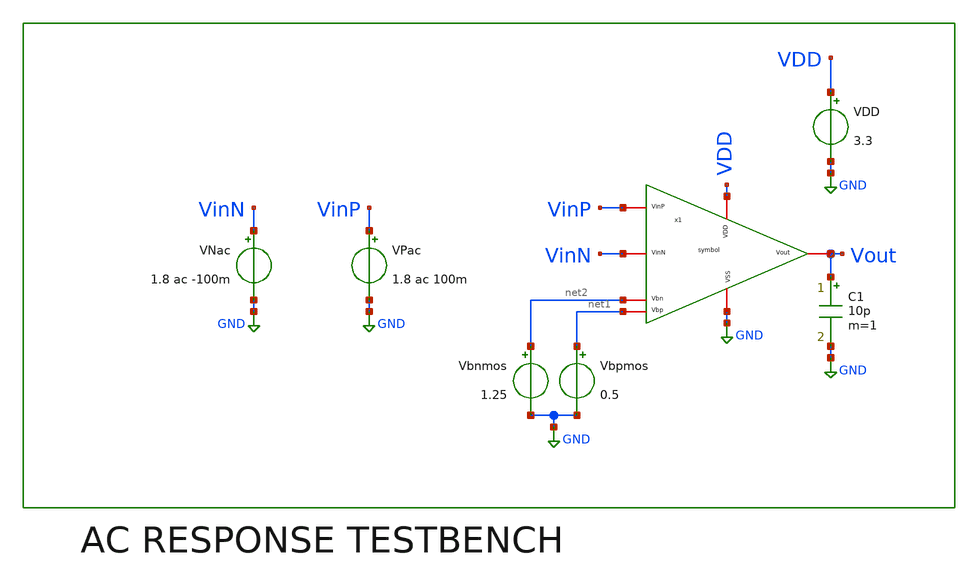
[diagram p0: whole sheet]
** sch_path: v2_bmr_bias/ACsim.sch
**.subckt ACsim
x1 VDD net1 VinP VinN Vout net2 GND symbol
VPac VinP GND 1.8 ac 100m
VNac VinN GND 1.8 ac -100m
Vbnmos net2 GND 1.25
Vbpmos net1 GND 0.5
VDD VDD GND 3.3
C1 Vout GND 10p m=1
**** begin user architecture code


.control
destroy all

ac dec 20 1 100Meg
run

let VinDiff = v(VinP) - v(VinN)
let gain_db = db(Vout/VinDiff)
let gain_phase = phase(Vout/VinDiff)*180/PI

save all

meas ac dc_gain      find gain_db at=1
meas ac f3db         when gain_db='dc_gain-3'
meas ac gbw          when gain_db=0
meas ac phase_at_gbw find gain_phase when gain_db=0
let phase_margin = 180 + phase_at_gbw

plot gain_db
plot gain_phase
plot gain_db gain_phase

print dc_gain
print f3db
print gbw
print phase_margin
.endc


**** end user architecture code
**.ends

* expanding   symbol:  /foss/designs/FOLDED/symbol.sym # of pins=7
** sym_path: v2_bmr_bias/symbol.sym
** sch_path: v2_bmr_bias/symbol.sch
.subckt symbol VDD Vbp VinP VinN Vout Vbn VSS
*.iopin Vbn
*.iopin Vbp
*.iopin VinP
*.iopin VinN
*.iopin Vout
*.iopin VDD
*.iopin VSS
XM1 net10 VinP net1 VSS sg13_hv_nmos w=7u l=1u ng=1 m=4 mm_ok=1
XM2 net9 VinN net1 VSS sg13_hv_nmos w=7u l=1u ng=1 m=4 mm_ok=1
XM3 net1 net3 VSS VSS sg13_hv_nmos w=3.75u l=1u ng=1 m=4 mm_ok=1
XM4 net10 net5 VDD VDD sg13_hv_pmos w=3.5u l=1u ng=1 m=4 mm_ok=1
XM5 net9 net5 VDD VDD sg13_hv_pmos w=3.5u l=1u ng=1 m=4 mm_ok=1
XM6 net2 Vbp net10 VDD sg13_hv_pmos w=4u l=1u ng=1 m=3 mm_ok=1
XM7 Vout Vbp net9 VDD sg13_hv_pmos w=4u l=1u ng=1 m=3 mm_ok=1
XM8 net2 Vbn net11 VSS sg13_hv_nmos w=7u l=1u ng=1 m=1 mm_ok=1
XM9 Vout Vbn net12 VSS sg13_hv_nmos w=7u l=1u ng=1 m=1 mm_ok=1
XM10 net11 net2 VSS VSS sg13_hv_nmos w=7u l=1u ng=1 m=1 mm_ok=1
XM11 net12 net2 VSS VSS sg13_hv_nmos w=7u l=1u ng=1 m=1 mm_ok=1
**** begin user architecture code



.lib cornerMOShv.lib mos_tt



**** end user architecture code
XM25 net3 net5 VDD VDD sg13_hv_pmos w=3.5u l=1u ng=1 m=1 mm_ok=1
XM12 net3 net3 VSS VSS sg13_hv_nmos w=3.75u l=1u ng=1 m=1 mm_ok=1
R1 net7 VSS 8.64k m=1
XM14 net8 net6 net7 VSS sg13_hv_nmos w=15u l=1u ng=2 m=1 mm_ok=1
XM15 net6 net6 VSS VSS sg13_hv_nmos w=3.75u l=1u ng=1 m=1 mm_ok=1
XM17 net6 net5 VDD VDD sg13_hv_pmos w=3.5u l=1u ng=1 m=1 mm_ok=1
XM18 net8 net5 VDD VDD sg13_hv_pmos w=3.5u l=1u ng=1 m=1 mm_ok=1
XM19 net4 net8 VSS VSS sg13_hv_nmos w=3.75u l=1u ng=1 m=1 mm_ok=1
XM20 net5 net6 VSS VSS sg13_hv_nmos w=3.75u l=1u ng=1 m=1 mm_ok=1
XM21 net4 net4 VDD VDD sg13_hv_pmos w=3.5u l=1u ng=1 m=1 mm_ok=1
XM22 net5 net4 VDD VDD sg13_hv_pmos w=3.5u l=1u ng=1 m=1 mm_ok=1
.ends

.GLOBAL GND
.end
